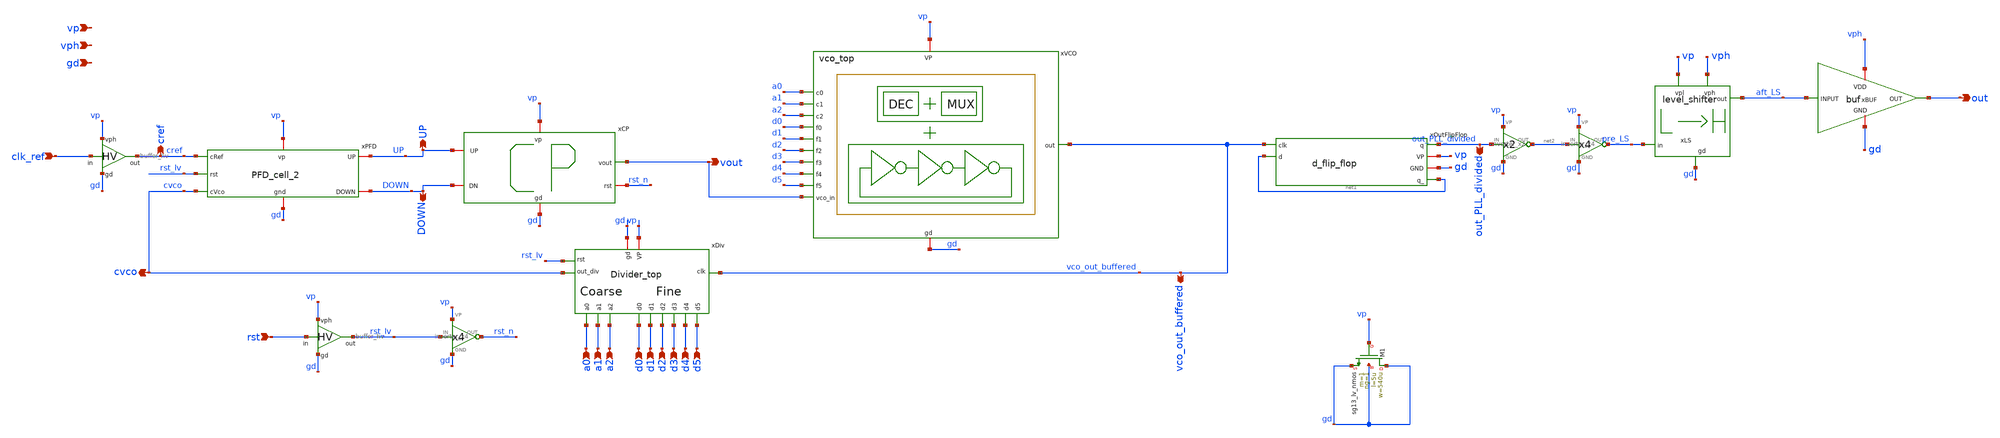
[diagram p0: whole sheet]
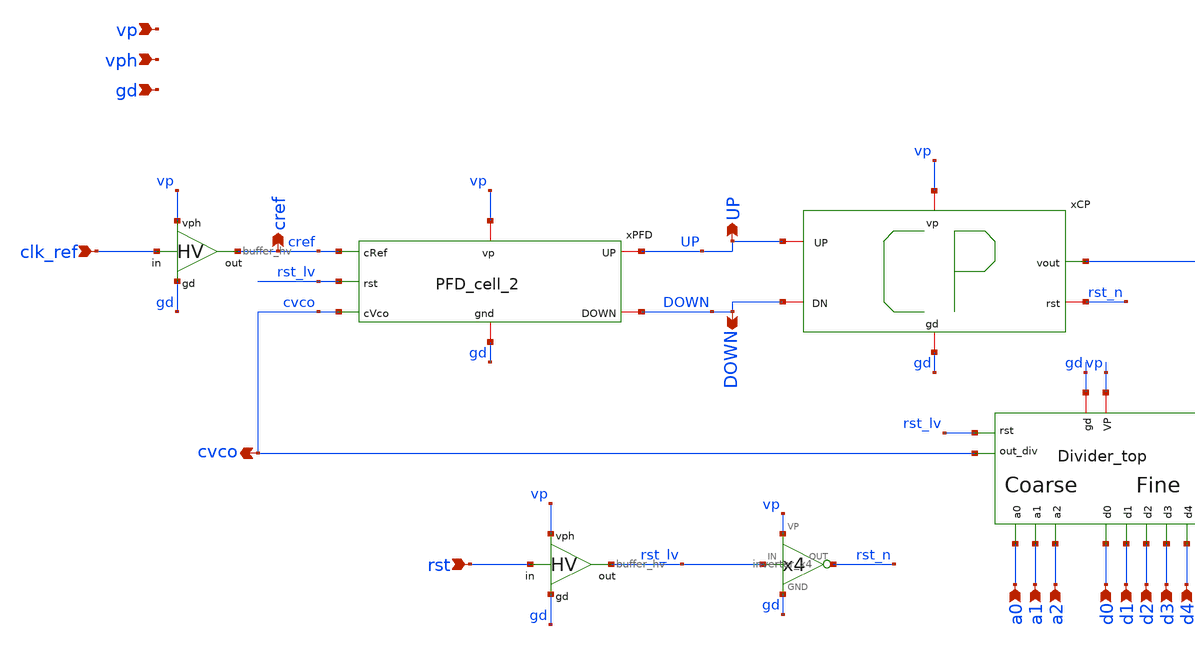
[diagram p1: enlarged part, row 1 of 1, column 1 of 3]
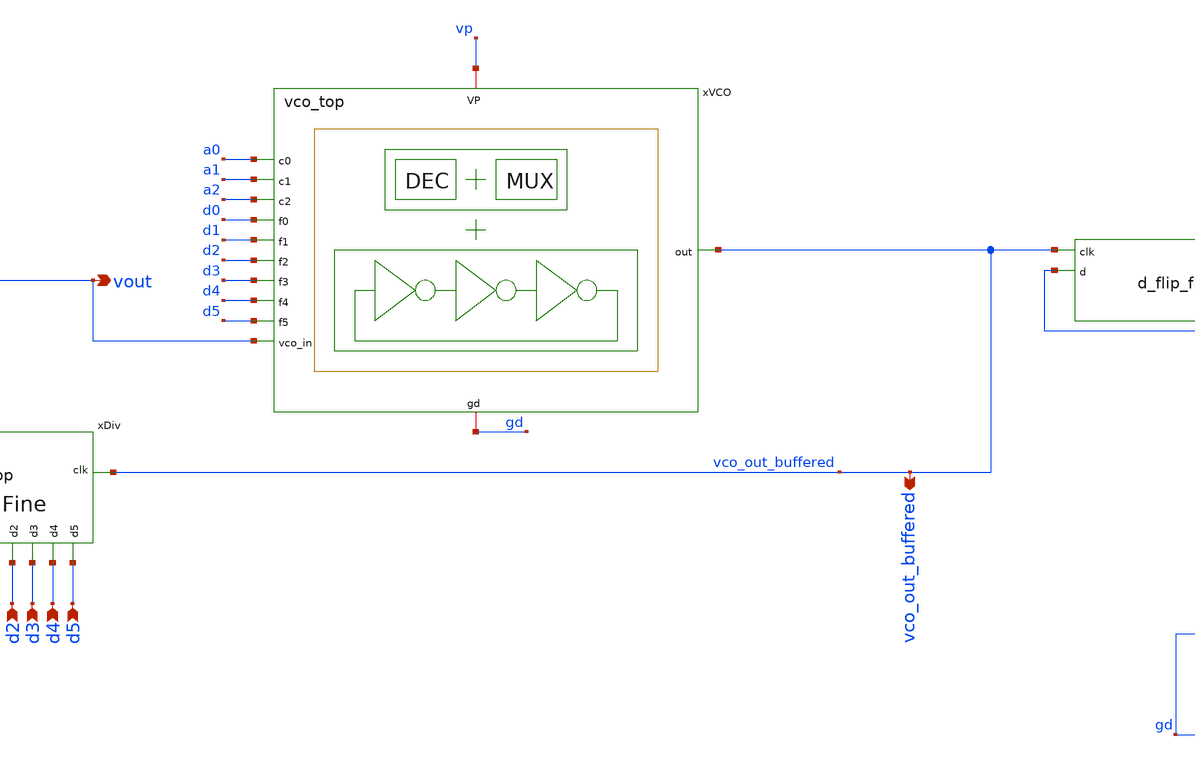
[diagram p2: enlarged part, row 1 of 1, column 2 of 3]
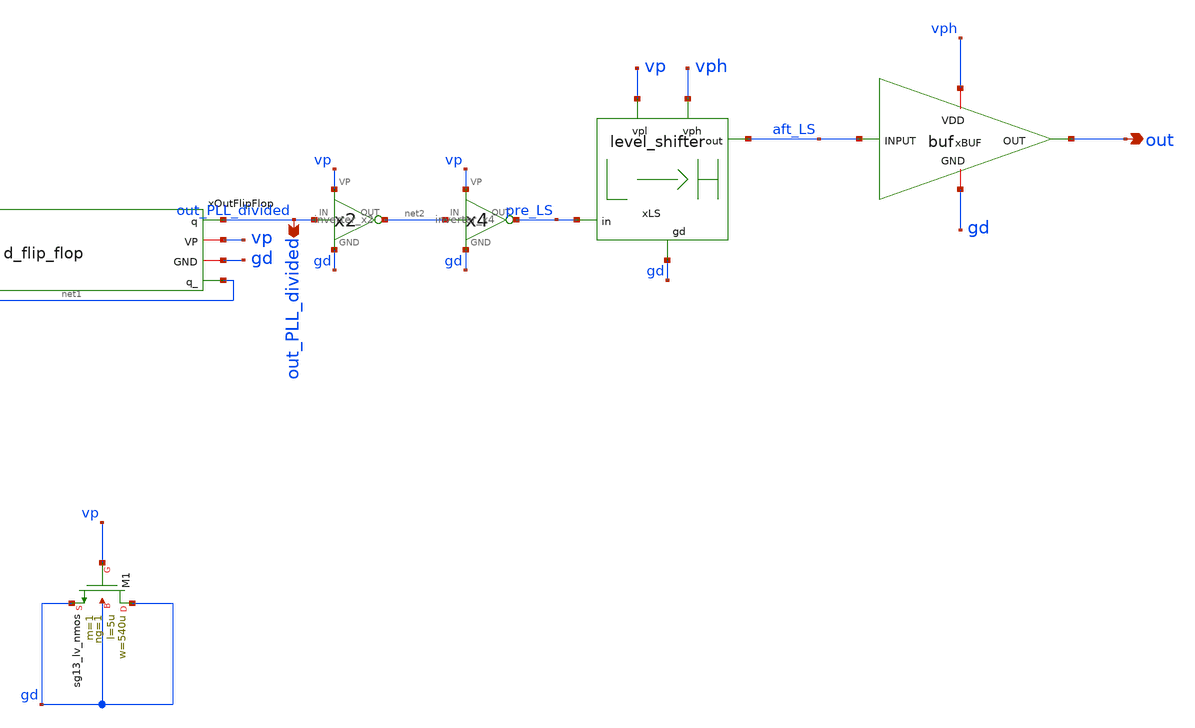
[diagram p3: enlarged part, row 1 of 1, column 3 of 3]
** sch_path: schematics/top/PLL_top.sch
**.subckt PLL_top clk_ref out gd vph vp a0 a1 a2 d0 d1 d2 d3 d4 d5 rst vout UP DOWN cvco
*+ vco_out_buffered out_PLL_divided cref
*.ipin clk_ref
*.opin out
*.ipin gd
*.ipin vph
*.ipin vp
*.ipin a0
*.ipin a1
*.ipin a2
*.ipin d0
*.ipin d1
*.ipin d2
*.ipin d3
*.ipin d4
*.ipin d5
*.ipin rst
*.opin vout
*.opin UP
*.opin DOWN
*.opin cvco
*.opin vco_out_buffered
*.opin out_PLL_divided
*.opin cref
x2 vp clk_ref cref gd buffer_hv
xPFD gd vp cref UP DOWN cvco rst_lv PFD_cell_2
xBUF vph aft_LS out gd buf
xDiv gd vp vco_out_buffered d0 d1 d2 d3 d4 d5 a0 a1 a2 cvco rst_lv Divider_top
xOutFlipFlop out_PLL_divided vp gd net1 vco_out_buffered net1 d_flip_flop
xLS vph aft_LS vp pre_LS gd level_shifter
x1 out_PLL_divided net2 vp gd inverter_x2
x3 net2 pre_LS vp gd inverter_x4
xCP vp UP vout DOWN rst_n gd charge_pump_cell
x9 rst_lv rst_n vp gd inverter_x4
xVCO vco_out_buffered gd vp a0 a1 a2 d0 d1 d2 d3 d4 d5 vout vco_top
x4 vp rst rst_lv gd buffer_hv
XM1 gd vp gd gd sg13_lv_nmos w=540u l=5u ng=1 m=1 mm_ok=1
**.ends
.end
